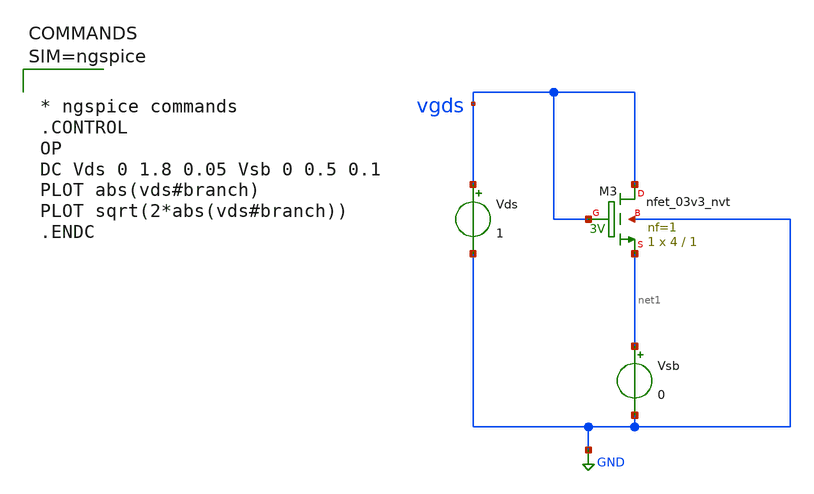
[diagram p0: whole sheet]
** sch_path: work/xschem/param_extract3.sch
**.subckt param_extract3
Vds vgds GND 1
Vsb net1 GND 0
XM3 vgds vgds net1 GND sky130_fd_pr__nfet_03v3_nvt L=1 W=4 nf=1 ad='int((1 + 1)/2) * 4 / 1 * 0.29' as='int((1 + 2)/2) * 4 / 1 * 0.29'
+ pd='2*int((1 + 1)/2) * (4 / 1 + 0.29)' ps='2*int((1 + 2)/2) * (4 / 1 + 0.29)' nrd='0.29 / 4 ' nrs='0.29 / 4 '
+ sa=0 sb=0 sd=0 mult=1 m=1
**** begin user architecture code



* ngspice commands
.CONTROL
OP
DC Vds 0 1.8 0.05 Vsb 0 0.5 0.1
PLOT abs(vds#branch)
PLOT sqrt(2*abs(vds#branch))
.ENDC





** opencircuitdesign pdks install
.lib $::SKYWATER_MODELS/sky130.lib.spice tt

**** end user architecture code
**.ends
.GLOBAL GND
.end
